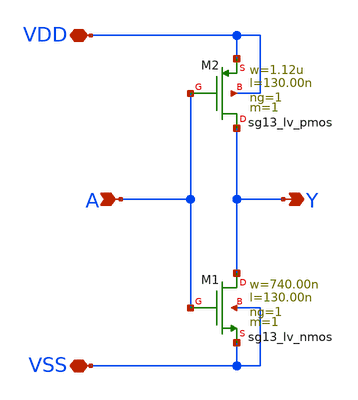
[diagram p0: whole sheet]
** sch_path: ihp-sg13g2/libs.tech/xschem/sg13g2_stdcells/sg13g2_inv_1.sch
**.subckt sg13g2_inv_1 Y A VDD VSS
*.opin Y
*.ipin A
*.iopin VDD
*.iopin VSS
XM1 Y A VSS VSS sg13_lv_nmos w=740.00n l=130.00n ng=1 m=1 mm_ok=1
XM2 Y A VDD VDD sg13_lv_pmos w=1.12u l=130.00n ng=1 m=1 mm_ok=1
**.ends
.end
